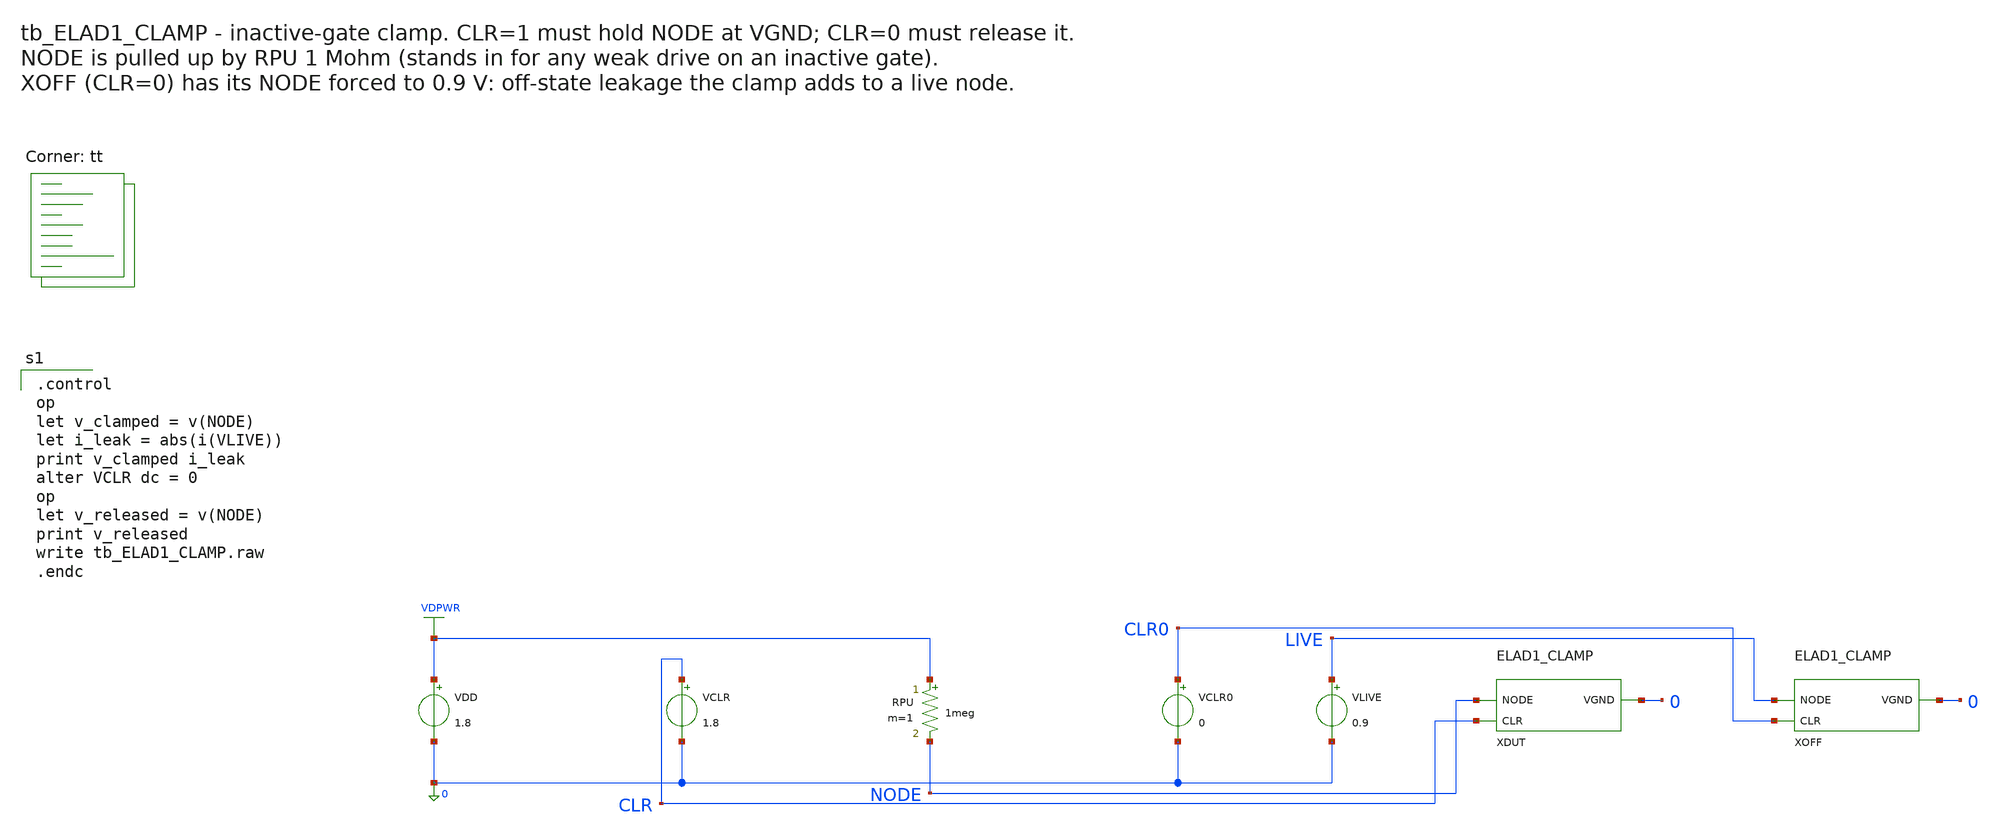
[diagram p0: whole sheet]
** sch_path: cells/ELAD1_CLAMP/schematic/tb_ELAD1_CLAMP.sch
**.subckt tb_ELAD1_CLAMP
VDD VDPWR 0 1.8
VCLR CLR 0 1.8
RPU VDPWR NODE 1meg m=1
XDUT NODE CLR 0 ELAD1_CLAMP
VCLR0 CLR0 0 0
VLIVE LIVE 0 0.9
XOFF LIVE CLR0 0 ELAD1_CLAMP
**** begin user architecture code

.control
op
let v_clamped = v(NODE)
let i_leak = abs(i(VLIVE))
print v_clamped i_leak
alter VCLR dc = 0
op
let v_released = v(NODE)
print v_released
write tb_ELAD1_CLAMP.raw
.endc

.lib $::SKYWATER_MODELS/sky130.lib.spice tt
**** end user architecture code
**.ends

* expanding   symbol:  ELAD1_CLAMP.sym # of pins=3
** sym_path: cells/ELAD1_CLAMP/schematic/ELAD1_CLAMP.sym
** sch_path: cells/ELAD1_CLAMP/schematic/ELAD1_CLAMP.sch
.subckt ELAD1_CLAMP NODE CLR VGND
*.iopin NODE
*.iopin CLR
*.iopin VGND
XM NODE CLR VGND VGND sky130_fd_pr__nfet_01v8 L=1 W=0.42 nf=1 ad='int((1 + 1)/2) * 0.42 / 1 * 0.29' as='int((1 + 2)/2) * 0.42 / 1 * 0.29'
+ pd='2*int((1 + 1)/2) * (0.42 / 1 + 0.29)' ps='2*int((1 + 2)/2) * (0.42 / 1 + 0.29)' nrd='0.29 / 0.42 '
+ nrs='0.29 / 0.42 ' sa=0 sb=0 sd=0 mult=1 m=1
.ends

.end
